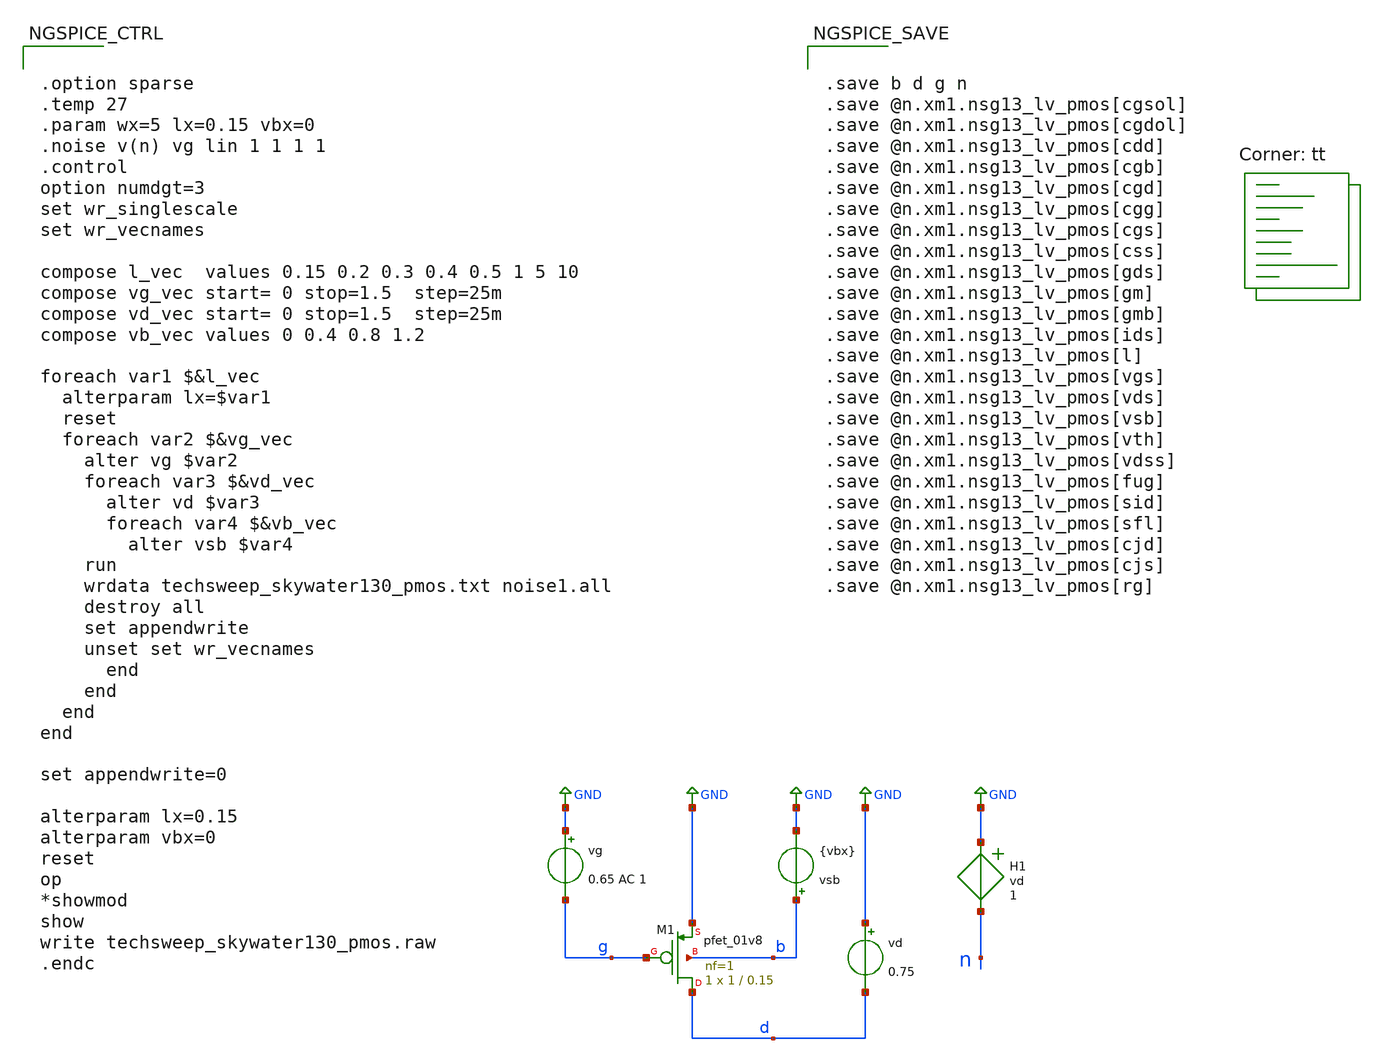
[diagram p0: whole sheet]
** sch_path: xschem/skywater130/techsweep_skywater130_pmos.sch
* (c) 2024 H. Pretl, Apache-2.0 license (adapted from B. Murmann)
**.subckt techsweep_skywater130_pmos
vd GND d 0.75
vsb b GND {vbx}
vg GND g 0.65 AC 1
H1 GND n vd 1
XM1 d g GND b sky130_fd_pr__pfet_01v8 L=0.15 W=1 nf=1 ad='int((nf+1)/2) * W/nf * 0.29' as='int((nf+2)/2) * W/nf * 0.29'
+ pd='2*int((nf+1)/2) * (W/nf + 0.29)' ps='2*int((nf+2)/2) * (W/nf + 0.29)' nrd='0.29 / W' nrs='0.29 / W'
+ sa=0 sb=0 sd=0 mult=1 m=1
**** begin user architecture code


.save b d g n
.save @n.xm1.nsg13_lv_pmos[cgsol]
.save @n.xm1.nsg13_lv_pmos[cgdol]
.save @n.xm1.nsg13_lv_pmos[cdd]
.save @n.xm1.nsg13_lv_pmos[cgb]
.save @n.xm1.nsg13_lv_pmos[cgd]
.save @n.xm1.nsg13_lv_pmos[cgg]
.save @n.xm1.nsg13_lv_pmos[cgs]
.save @n.xm1.nsg13_lv_pmos[css]
.save @n.xm1.nsg13_lv_pmos[gds]
.save @n.xm1.nsg13_lv_pmos[gm]
.save @n.xm1.nsg13_lv_pmos[gmb]
.save @n.xm1.nsg13_lv_pmos[ids]
.save @n.xm1.nsg13_lv_pmos[l]
.save @n.xm1.nsg13_lv_pmos[vgs]
.save @n.xm1.nsg13_lv_pmos[vds]
.save @n.xm1.nsg13_lv_pmos[vsb]
.save @n.xm1.nsg13_lv_pmos[vth]
.save @n.xm1.nsg13_lv_pmos[vdss]
.save @n.xm1.nsg13_lv_pmos[fug]
.save @n.xm1.nsg13_lv_pmos[sid]
.save @n.xm1.nsg13_lv_pmos[sfl]
.save @n.xm1.nsg13_lv_pmos[cjd]
.save @n.xm1.nsg13_lv_pmos[cjs]
.save @n.xm1.nsg13_lv_pmos[rg]




.option sparse
.temp 27
.param wx=5 lx=0.15 vbx=0
.noise v(n) vg lin 1 1 1 1
.control
option numdgt=3
set wr_singlescale
set wr_vecnames

compose l_vec  values 0.15 0.2 0.3 0.4 0.5 1 5 10
compose vg_vec start= 0 stop=1.5  step=25m
compose vd_vec start= 0 stop=1.5  step=25m
compose vb_vec values 0 0.4 0.8 1.2

foreach var1 $&l_vec
  alterparam lx=$var1
  reset
  foreach var2 $&vg_vec
    alter vg $var2
    foreach var3 $&vd_vec
      alter vd $var3
      foreach var4 $&vb_vec
        alter vsb $var4
	run
	wrdata techsweep_skywater130_pmos.txt noise1.all
	destroy all
	set appendwrite
	unset set wr_vecnames
      end
    end
  end
end

set appendwrite=0

alterparam lx=0.15
alterparam vbx=0
reset
op
*showmod
show
write techsweep_skywater130_pmos.raw
.endc


.lib $::SKYWATER_MODELS/sky130.lib.spice tt
**** end user architecture code
**.ends
.GLOBAL GND
.end
